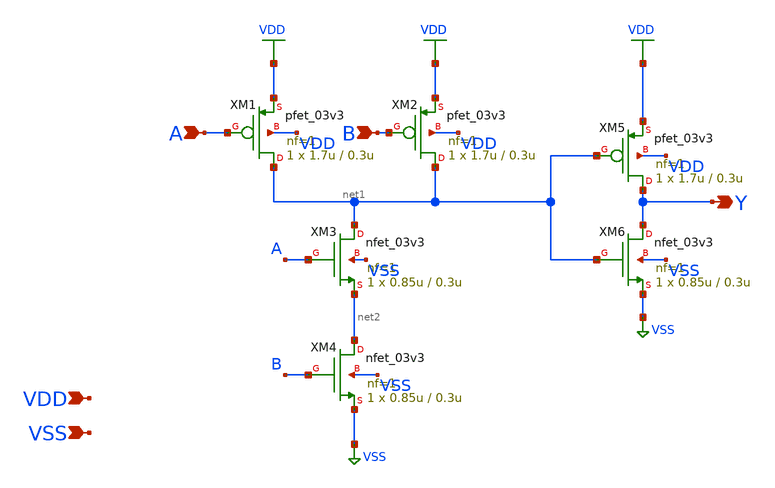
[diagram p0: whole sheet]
** sch_path: gf180mcu_osu_sc_gp12t3v3/xschem/gf180mcu_osu_sc_gp12t3v3__and2_1.sch
**.subckt gf180mcu_osu_sc_gp12t3v3__and2_1 A B Y VDD VSS
*.ipin A
*.ipin B
*.opin Y
*.ipin VDD
*.ipin VSS
XM1 net1 A VDD VDD pfet_03v3 L=0.3u W=1.7u nf=1 ad='int((nf+1)/2) * W/nf * 0.18u' as='int((nf+2)/2) * W/nf * 0.18u'
+ pd='2*int((nf+1)/2) * (W/nf + 0.18u)' ps='2*int((nf+2)/2) * (W/nf + 0.18u)' nrd='0.18u / W' nrs='0.18u / W'
+ sa=0 sb=0 sd=0 m=1
XM2 net1 B VDD VDD pfet_03v3 L=0.3u W=1.7u nf=1 ad='int((nf+1)/2) * W/nf * 0.18u' as='int((nf+2)/2) * W/nf * 0.18u'
+ pd='2*int((nf+1)/2) * (W/nf + 0.18u)' ps='2*int((nf+2)/2) * (W/nf + 0.18u)' nrd='0.18u / W' nrs='0.18u / W'
+ sa=0 sb=0 sd=0 m=1
XM3 net1 A net2 VSS nfet_03v3 L=0.3u W=0.85u nf=1 ad='int((nf+1)/2) * W/nf * 0.18u' as='int((nf+2)/2) * W/nf * 0.18u'
+ pd='2*int((nf+1)/2) * (W/nf + 0.18u)' ps='2*int((nf+2)/2) * (W/nf + 0.18u)' nrd='0.18u / W' nrs='0.18u / W'
+ sa=0 sb=0 sd=0 m=1
XM4 net2 B VSS VSS nfet_03v3 L=0.3u W=0.85u nf=1 ad='int((nf+1)/2) * W/nf * 0.18u' as='int((nf+2)/2) * W/nf * 0.18u'
+ pd='2*int((nf+1)/2) * (W/nf + 0.18u)' ps='2*int((nf+2)/2) * (W/nf + 0.18u)' nrd='0.18u / W' nrs='0.18u / W'
+ sa=0 sb=0 sd=0 m=1
XM5 Y net1 VDD VDD pfet_03v3 L=0.3u W=1.7u nf=1 ad='int((nf+1)/2) * W/nf * 0.18u' as='int((nf+2)/2) * W/nf * 0.18u'
+ pd='2*int((nf+1)/2) * (W/nf + 0.18u)' ps='2*int((nf+2)/2) * (W/nf + 0.18u)' nrd='0.18u / W' nrs='0.18u / W'
+ sa=0 sb=0 sd=0 m=1
XM6 Y net1 VSS VSS nfet_03v3 L=0.3u W=0.85u nf=1 ad='int((nf+1)/2) * W/nf * 0.18u' as='int((nf+2)/2) * W/nf * 0.18u'
+ pd='2*int((nf+1)/2) * (W/nf + 0.18u)' ps='2*int((nf+2)/2) * (W/nf + 0.18u)' nrd='0.18u / W' nrs='0.18u / W'
+ sa=0 sb=0 sd=0 m=1
**.ends
.GLOBAL VDD
.GLOBAL VSS
.end
